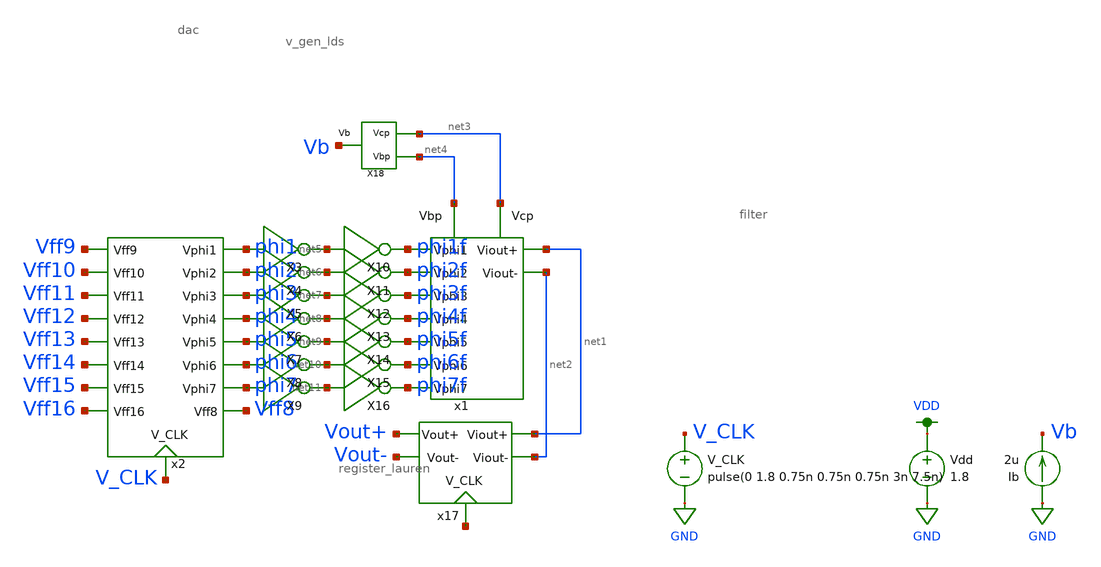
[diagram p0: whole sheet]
** sch_path: simulation/archived/register_dac_single_andrew.sch
**.subckt register_dac_single_andrew
V_CLK V_CLK GND pulse(0 1.8 0.75n 0.75n 0.75n 3n 7.5n)
Vdd VDD GND 1.8
x1 phi1f phi2f phi3f phi4f phi5f phi6f phi7f net1 net2 net4 net3 dac
x2 Vff10 Vff11 Vff12 Vff13 Vff14 Vff16 Vff15 Vff9 phi1 phi2 phi3 phi4 phi5 phi6 phi7 Vff8 V_CLK
+ register_lauren
X3 phi1 net5 inverter
X4 phi2 net6 inverter
X5 phi3 net7 inverter
X6 phi4 net8 inverter
X7 phi5 net9 inverter
X8 phi6 net10 inverter
X9 phi7 net11 inverter
X10 net5 phi1f inverter
X11 net6 phi2f inverter
X12 net7 phi3f inverter
X13 net8 phi4f inverter
X14 net9 phi5f inverter
X15 net10 phi6f inverter
X16 net11 phi7f inverter
x17 net1 net2 Vout+ Vout- net12 filter
X18 net3 net4 Vb v_gen_lds
Ib GND Vb 2u
**** begin user architecture code

.option wnflag=1
.param MC_SWITCH=0.0
.lib ~/skywater/skywater-pdk/libraries/sky130_fd_pr_ngspice/latest/models/sky130.lib.spice tt



.ic v(phi1)=0 v(phi2)=0 v(phi3)=0 v(phi4)=0 v(phi5)=0 v(phi6)=0 v(phi7)=0 v(Vff8)=0 v(Vff9)=1.8
+ v(Vff10)=1.8 v(Vff11)=1.8 v(Vff12)=1.8 v(Vff13)=1.8 v(Vff14)=1.8 v(Vff15)=1.8 v(Vff16)=1.8
.control
  set wr_vecnames
  set wr_singlescale

  let mc_runs = 10
  let run = 1
  dowhile run <= mc_runs
    tran 0.1n 1u
    wrdata ~/Documents/VLSI_Sine_Gen/simulation/sim_data/register_dac_single_7_5ns.txt v(Vout+)
+ v(Vout-) v(Vout+)-v(Vout-)
    reset
    let run = run + 1
  end
  quit
.endc


**** end user architecture code
**.ends
.GLOBAL GND
.GLOBAL VDD
.end
